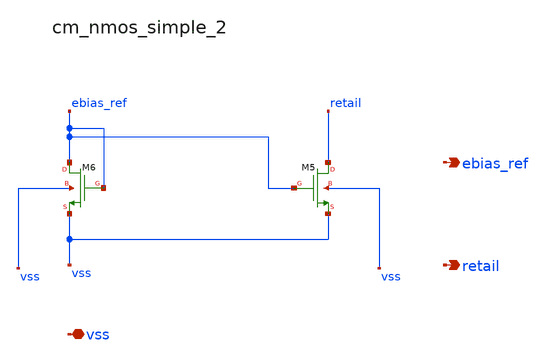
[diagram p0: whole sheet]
** sch_path: analog-db/raw/ldo_005_buffered_ref/hier/blocks/cm_nmos_simple_2.sch
**.subckt cm_nmos_simple_2 vss ebias_ref retail
*.iopin vss
*.opin ebias_ref
*.opin retail
XM5 retail ebias_ref vss vss sg13_lv_nmos w=x_dut_xm5_w l=x_dut_xm5_l ng=1 m=1
XM6 ebias_ref ebias_ref vss vss sg13_lv_nmos w=x_dut_xm6_w l=x_dut_xm6_l ng=1 m=1
**.ends
.end
